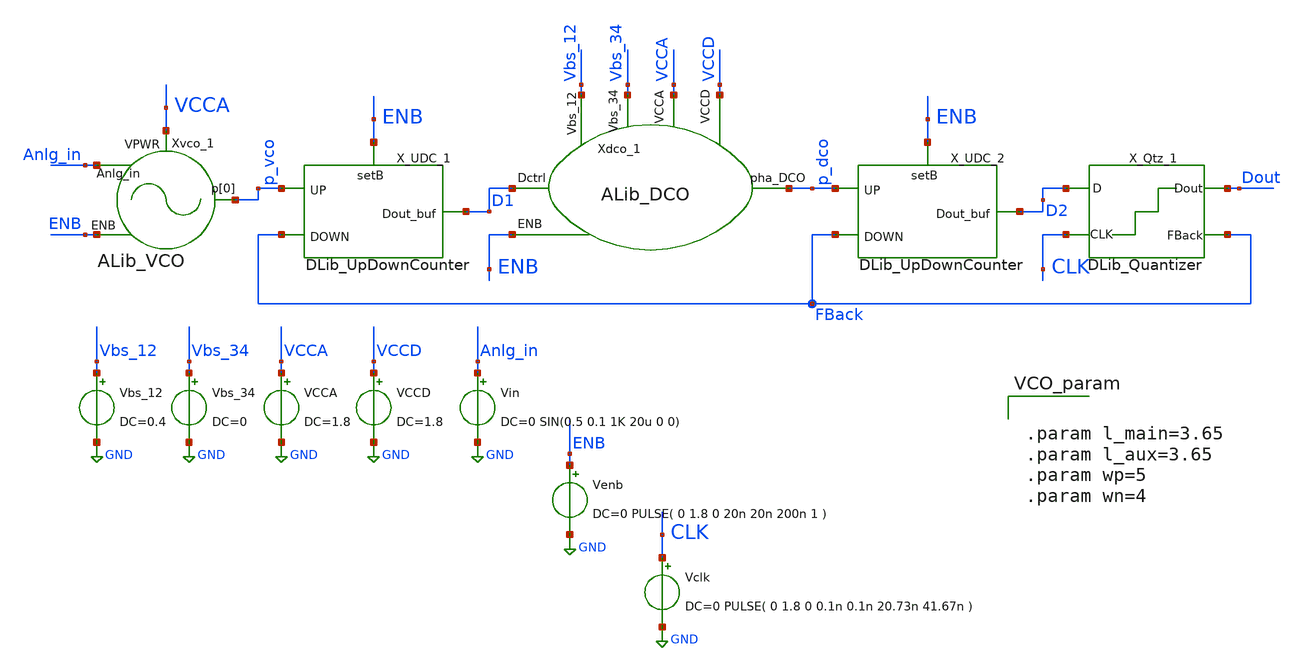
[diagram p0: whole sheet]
** sch_path: xschem/tb/VCO_ADC_tb.sch

.include $::SKYWATER_STDCELLS/sky130_fd_sc_hd.spice
.lib $::SKYWATER_MODELS/sky130.lib.spice tt

**.subckt VCO_ADC_tb
Vbs_34 Vbs_34 GND DC=0
VCCA VCCA GND DC=1.8
VCCD VCCD GND DC=1.8
Vin Anlg_in GND DC=0 SIN(0.5 0.1 1K 20u 0 0)
Venb ENB GND DC=0 PULSE( 0 1.8 0 20n 20n 200n 1 )
Vclk CLK GND DC=0 PULSE( 0 1.8 0 0.1n 0.1n 20.73n 41.67n )
Vbs_12 Vbs_12 GND DC=0.4
Xdco_1 D1 ENB Vbs_12 Vbs_34 VCCD VCCA p_dco ALib_DCO
Xvco_1 VCCA p_vco Anlg_in ENB ALib_VCO L12=0.15 Wp12=2.4 Wn12=1.2 L34=0.15 Wp34=1.2 Wn34=0.65
X_UDC_1 p_vco FBack ENB GND GND VCCD VCCD D1 DLib_UpDownCounter
X_Qtz_1 CLK D2 GND GND VCCD VCCD Dout FBack DLib_Quantizer
X_UDC_2 p_dco FBack ENB GND GND VCCD VCCD D2 DLib_UpDownCounter
**.ends
.GLOBAL GND
**** begin user architecture code


.control
   set num_threads=8
   tran 0.5n 10u
   plot p_vco/2+6 D1/2+5 p_dco/2+4 Xdco_1.p_osc/2+4 CLK/2+3 D2/2+2 Dout/2+1 FBack/2+0.05
.endc




.param l_main=3.65
.param l_aux=3.65
.param wp=5
.param wn=4

**** end user architecture code
.end
